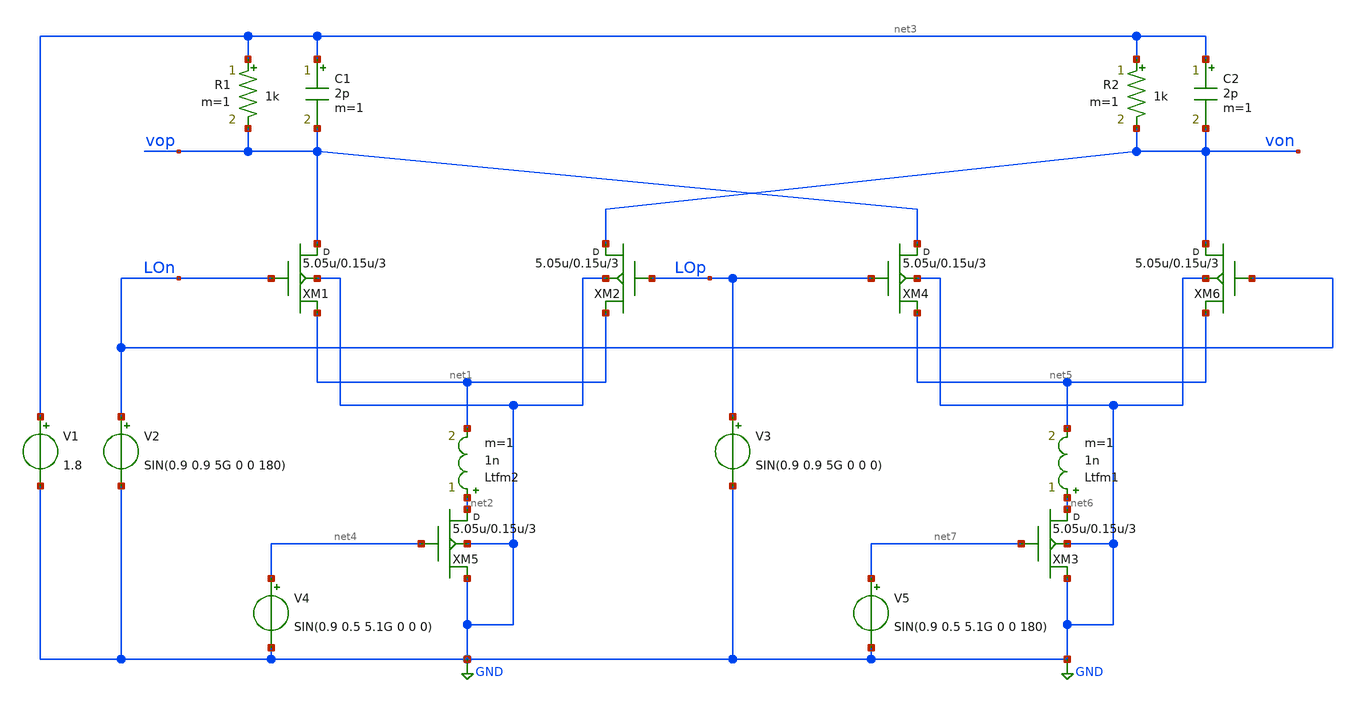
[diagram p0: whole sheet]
** sch_path: xschem/mixer_5G.sch
**.subckt mixer_5G
XM5 net2 net4 GND GND sky130_fd_pr__rf_nfet_01v8_bM04W5p00L0p15_ext w=5.05u l=0.15u m=3
XM1 vop LOn net1 GND sky130_fd_pr__rf_nfet_01v8_bM04W5p00L0p15_ext w=5.05u l=0.15u m=3
XM2 von LOp net1 GND sky130_fd_pr__rf_nfet_01v8_bM04W5p00L0p15_ext w=5.05u l=0.15u m=3
Ltfm2 net2 net1 1n m=1
C1 net3 vop 2p m=1
R1 net3 vop 1k m=1
C2 net3 von 2p m=1
R2 net3 von 1k m=1
V1 net3 GND 1.8
V2 LOn GND SIN(0.9 0.9 5G 0 0 180)
V3 LOp GND SIN(0.9 0.9 5G 0 0 0)
V4 net4 GND SIN(0.9 0.5 5.1G 0 0 0)
XM3 net6 net7 GND GND sky130_fd_pr__rf_nfet_01v8_bM04W5p00L0p15_ext w=5.05u l=0.15u m=3
XM4 vop LOp net5 GND sky130_fd_pr__rf_nfet_01v8_bM04W5p00L0p15_ext w=5.05u l=0.15u m=3
XM6 von LOn net5 GND sky130_fd_pr__rf_nfet_01v8_bM04W5p00L0p15_ext w=5.05u l=0.15u m=3
Ltfm1 net6 net5 1n m=1
V5 net7 GND SIN(0.9 0.5 5.1G 0 0 180)
**** begin user architecture code


.subckt sky130_fd_pr__rf_nfet_01v8_bM04W5p00L0p15_ext DRAIN GATE SOURCE SUBSTRATE
X0 DRAIN GATE SOURCE SUBSTRATE sky130_fd_pr__nfet_01v8 ad=2.828e+12p pd=2.132e+07u as=4.242e+12p
+ ps=3.198e+07u w=5.05e+06u l=150000u
X1 SOURCE SUBSTRATE SUBSTRATE SUBSTRATE sky130_fd_pr__nfet_01v8 ad=0p pd=0u as=3.03e+12p
+ ps=2.14e+07u w=5.05e+06u l=150000u
X2 SOURCE GATE DRAIN SUBSTRATE sky130_fd_pr__nfet_01v8 ad=0p pd=0u as=0p ps=0u w=5.05e+06u l=150000u
X3 DRAIN GATE SOURCE SUBSTRATE sky130_fd_pr__nfet_01v8 ad=0p pd=0u as=0p ps=0u w=5.05e+06u l=150000u
X4 SUBSTRATE SUBSTRATE SOURCE SUBSTRATE sky130_fd_pr__nfet_01v8 ad=0p pd=0u as=0p ps=0u w=5.05e+06u
+ l=150000u
X5 SOURCE GATE DRAIN SUBSTRATE sky130_fd_pr__nfet_01v8 ad=0p pd=0u as=0p ps=0u w=5.05e+06u l=150000u
.ends
.options savecurrents
.tran 0.1ps 100ns
.control
run
display
plot v(von)
plot v(nmid)
.endc


.lib $::SKYWATER_MODELS/sky130.lib.spice ss
* .include $::PDKPATH/libs.ref/sky130_fd_sc_hvl/spice/sky130_fd_sc_hvl.spice

**** end user architecture code
**.ends
.GLOBAL GND
.end
